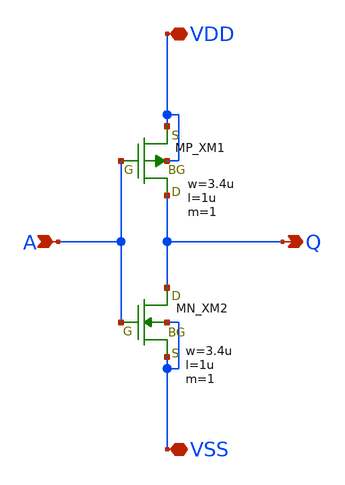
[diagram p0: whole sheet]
** sch_path: member_project/inverter/ichiken/TadasukeKuramochi/inverter_TadasukeKuramochi.sch
**.subckt inverter_TadasukeKuramochi A Q VDD VSS
*.ipin A
*.opin Q
*.iopin VDD
*.iopin VSS
XXM1 Q A VDD VDD PMOS w=3.4u l=1u as=0 ad=0 ps=0 pd=0 nrd=0 nrs=0 m=1
XXM2 Q A VSS VSS NMOS w=3.4u l=1u as=0 ad=0 ps=0 pd=0 nrd=0 nrs=0 m=1
**.ends
.end
